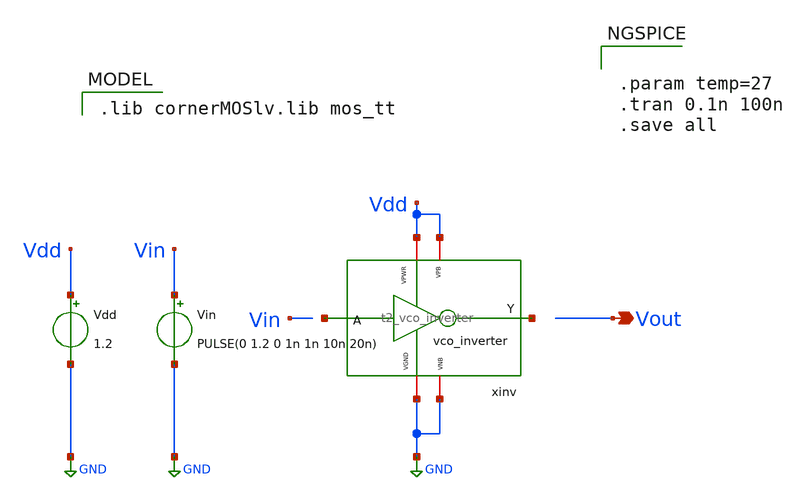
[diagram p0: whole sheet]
** sch_path: Team Designs/Team 2 Design/design_data/xschem/t2_vco_inverter_tb_pulse.sch
**.subckt t2_vco_inverter_tb_pulse Vout
*.opin Vout
Vin Vin GND PULSE(0 1.2 0 1n 1n 10n 20n)
Vdd Vdd GND 1.2
x1 Vdd Vdd net1 net2 GND GND t2_vco_inverter
**** begin user architecture code
 .lib cornerMOSlv.lib mos_tt



.param temp=27
.tran 0.1n 100n
.save all


**** end user architecture code
**.ends

* expanding   symbol:  /foss/designs/cmos-pll-ihp-sg13g2/Team 2
*+ Design/design_data/xschem/t2_vco_inverter.sym # of pins=6
** sym_path: Team 2 Design/design_data/xschem/t2_vco_inverter.sym
** sch_path: Team 2 Design/design_data/xschem/t2_vco_inverter.sch
.subckt t2_vco_inverter VPWR VPB A Y VNB VGND
*.iopin VPWR
*.iopin VGND
*.ipin A
*.opin Y
*.iopin VPB
*.iopin VNB
XM2 Y A VPWR VPB sg13_lv_pmos w=1u l=0.13u ng=1 m=1 mm_ok=1
XM1 Y A VGND VNB sg13_lv_nmos w=0.5u l=0.13u ng=1 m=1 mm_ok=1
.ends

.GLOBAL GND
.end
